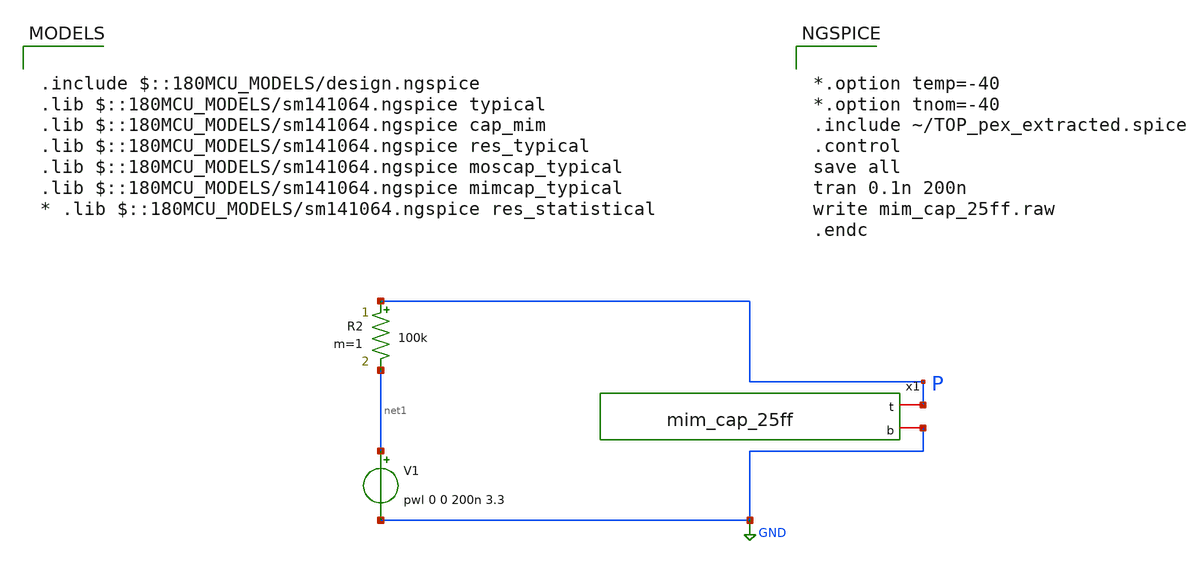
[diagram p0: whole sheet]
** sch_path: noritsuna/CDAC/Bo-Yu_Tseng/mim_cap_25ff.sch
**.subckt mim_cap_25ff
R2 P net1 100k m=1
V1 net1 GND pwl 0 0 200n 3.3
x1 P GND TOP
**** begin user architecture code

.include $::180MCU_MODELS/design.ngspice
.lib $::180MCU_MODELS/sm141064.ngspice typical
.lib $::180MCU_MODELS/sm141064.ngspice cap_mim
.lib $::180MCU_MODELS/sm141064.ngspice res_typical
.lib $::180MCU_MODELS/sm141064.ngspice moscap_typical
.lib $::180MCU_MODELS/sm141064.ngspice mimcap_typical
* .lib $::180MCU_MODELS/sm141064.ngspice res_statistical



*.option temp=-40
*.option tnom=-40
.include ~/TOP_pex_extracted.spice
.control
save all
tran 0.1n 200n
write mim_cap_25ff.raw
.endc


**** end user architecture code
**.ends
.GLOBAL GND
.end
